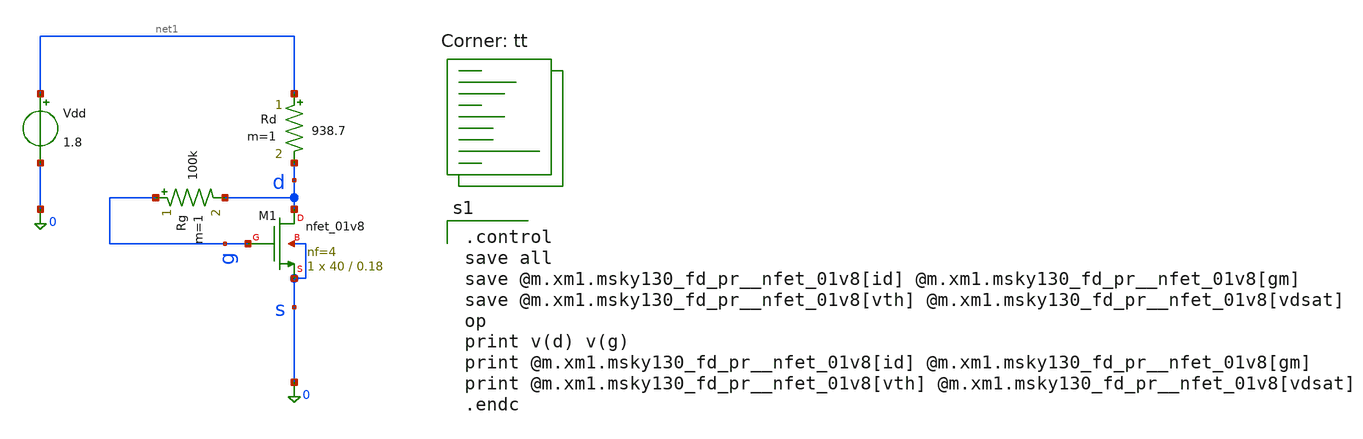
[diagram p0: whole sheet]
** sch_path: Homework 4 - Differential Pair Small Signal Gain/Simulations/ex3_final.sch
**.subckt ex3_final
XM1 d g 0 0 sky130_fd_pr__nfet_01v8 L=0.18 W=40 nf=4 ad='int((4 + 1)/2) * 40 / 4 * 0.29' as='int((4 + 2)/2) * 40 / 4 * 0.29'
+ pd='2*int((4 + 1)/2) * (40 / 4 + 0.29)' ps='2*int((4 + 2)/2) * (40 / 4 + 0.29)' nrd='0.29 / 40 ' nrs='0.29 / 40 '
+ sa=0 sb=0 sd=0 mult=1 m=1
Vdd net1 0 1.8
Rd net1 d 938.7 m=1
Rg g d 100k m=1
**** begin user architecture code
.lib $::SKYWATER_MODELS/sky130.lib.spice tt

.control
save all
save @m.xm1.msky130_fd_pr__nfet_01v8[id] @m.xm1.msky130_fd_pr__nfet_01v8[gm]
save @m.xm1.msky130_fd_pr__nfet_01v8[vth] @m.xm1.msky130_fd_pr__nfet_01v8[vdsat]
op
print v(d) v(g)
print @m.xm1.msky130_fd_pr__nfet_01v8[id] @m.xm1.msky130_fd_pr__nfet_01v8[gm]
print @m.xm1.msky130_fd_pr__nfet_01v8[vth] @m.xm1.msky130_fd_pr__nfet_01v8[vdsat]
.endc

**** end user architecture code
**.ends
.end
